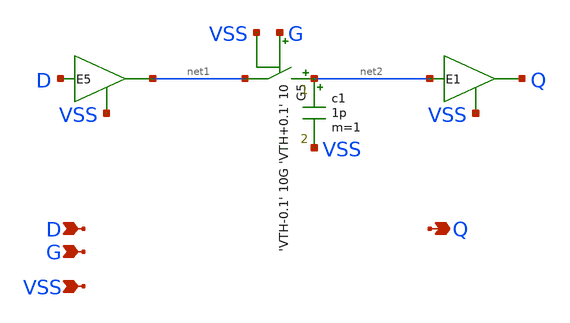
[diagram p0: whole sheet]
** sch_path: xschem_libs_newsym/examples/dlatch/schematic/dlatch.sch
* Copyright (C) 1998-2024 Stefan Frederik Schippers
* This program is free software; you can redistribute it and/or modify
* it under the terms of the GNU General Public License as published by
* the Free Software Foundation; either version 2 of the License, or
* (at your option) any later version.
* This program is distributed in the hope that it will be useful,
* but WITHOUT ANY WARRANTY; without even the implied warranty of
* MERCHANTABILITY or FITNESS FOR A PARTICULAR PURPOSE.  See the
* GNU General Public License for more details.
* You should have received a copy of the GNU General Public License
* along with this program; if not, write to the Free Software
**.subckt dlatch D Q VSS G
*.ipin D
*.opin Q
*.ipin VSS
*.ipin G
G5 net2 net1 vcr pwl(1) G VSS 'VTH-0.1' 10G 'VTH+0.1' 10
c1 net2 VSS 1p m=1
E5 net1 VSS pwl(1) D VSS 'VTH-0.1' 0 'VTH+0.1' VHI
E1 Q VSS pwl(1) net2 VSS 'VTH-0.1' 0 'VTH+0.1' VHI
**.ends
.end
